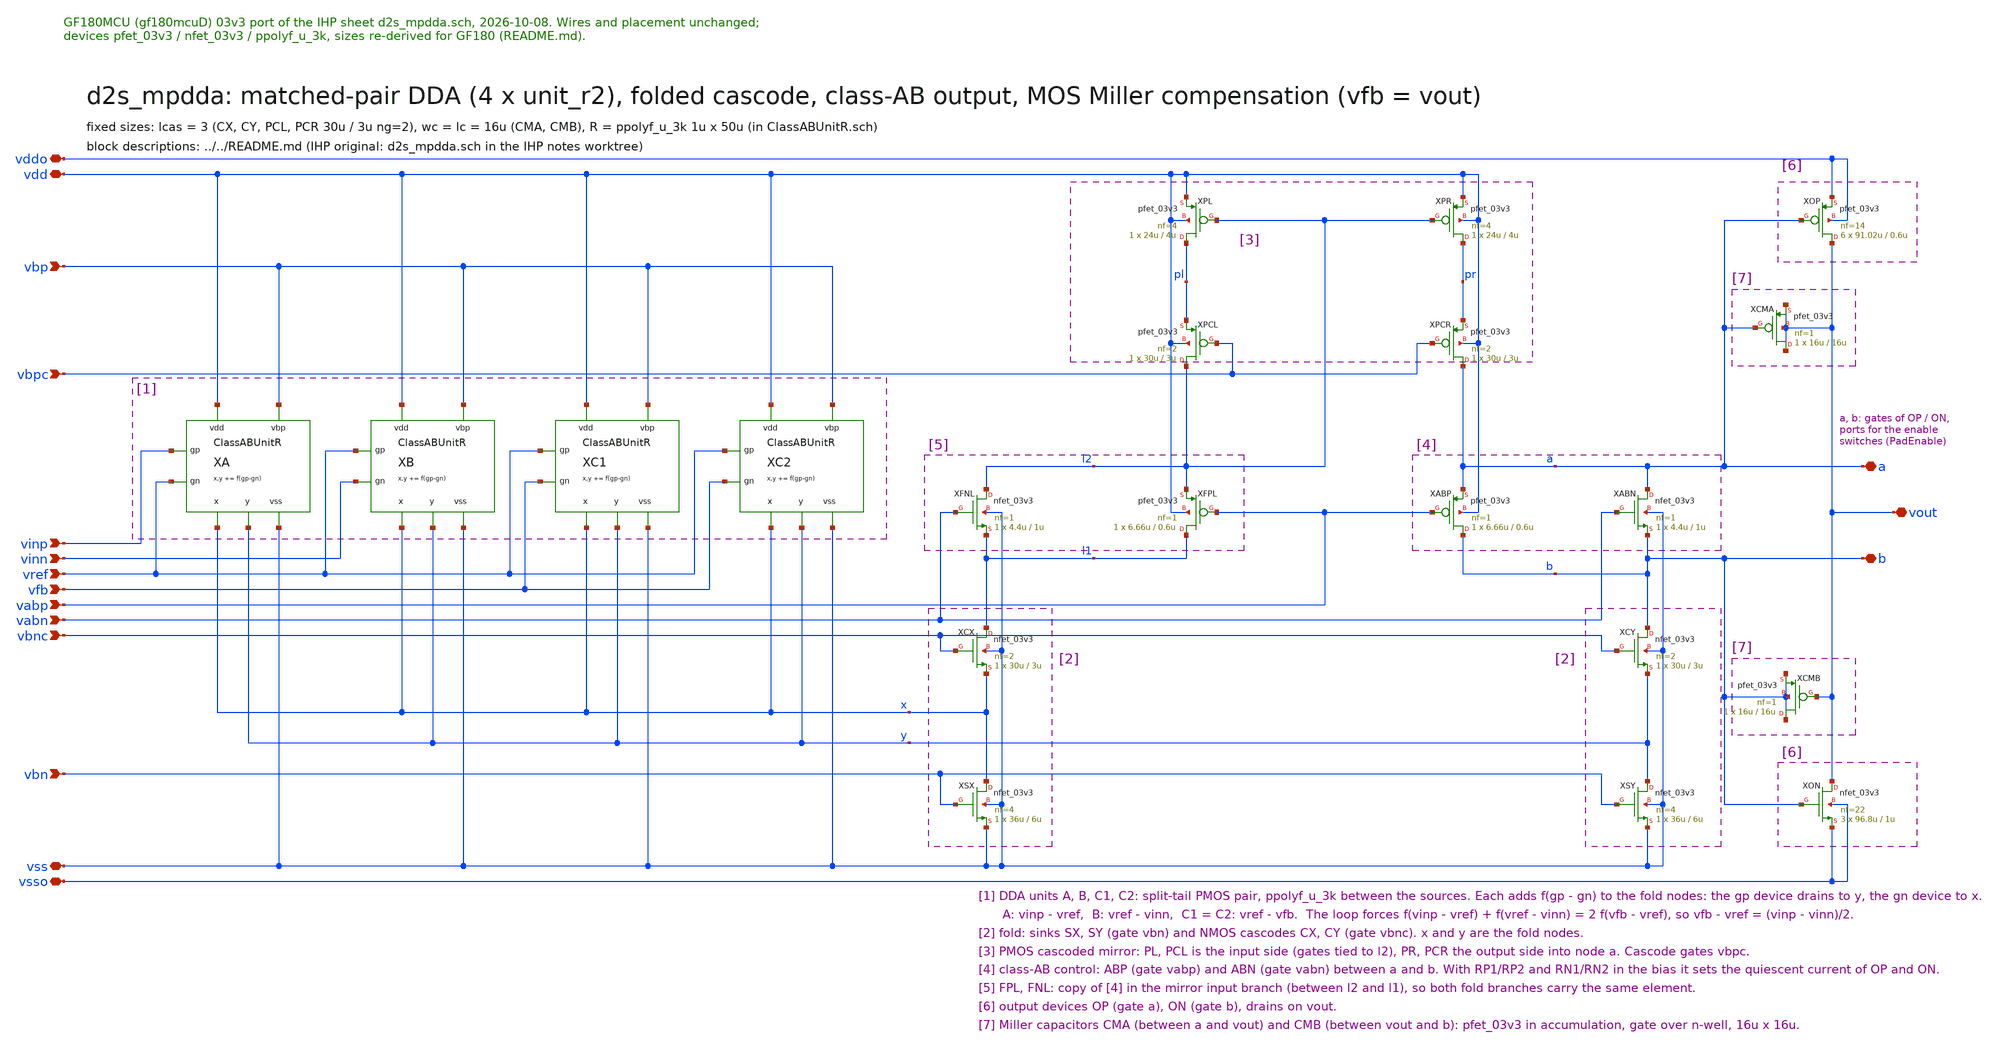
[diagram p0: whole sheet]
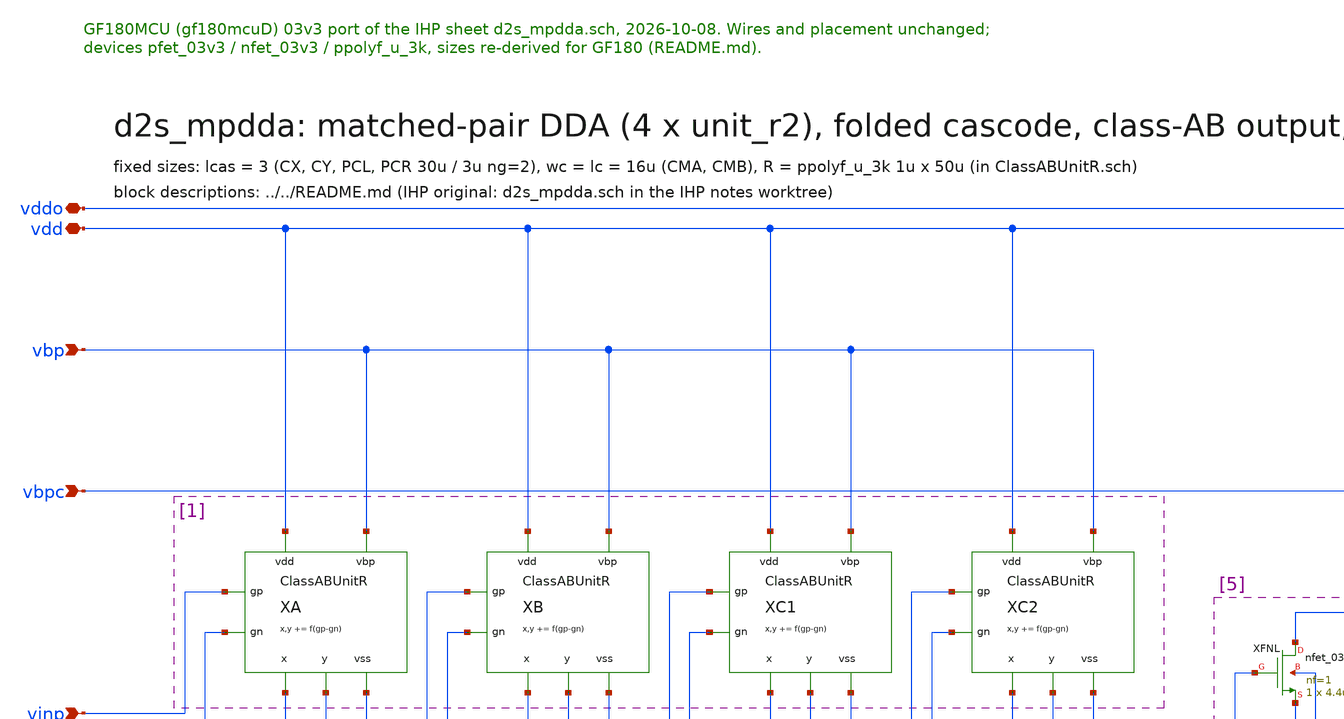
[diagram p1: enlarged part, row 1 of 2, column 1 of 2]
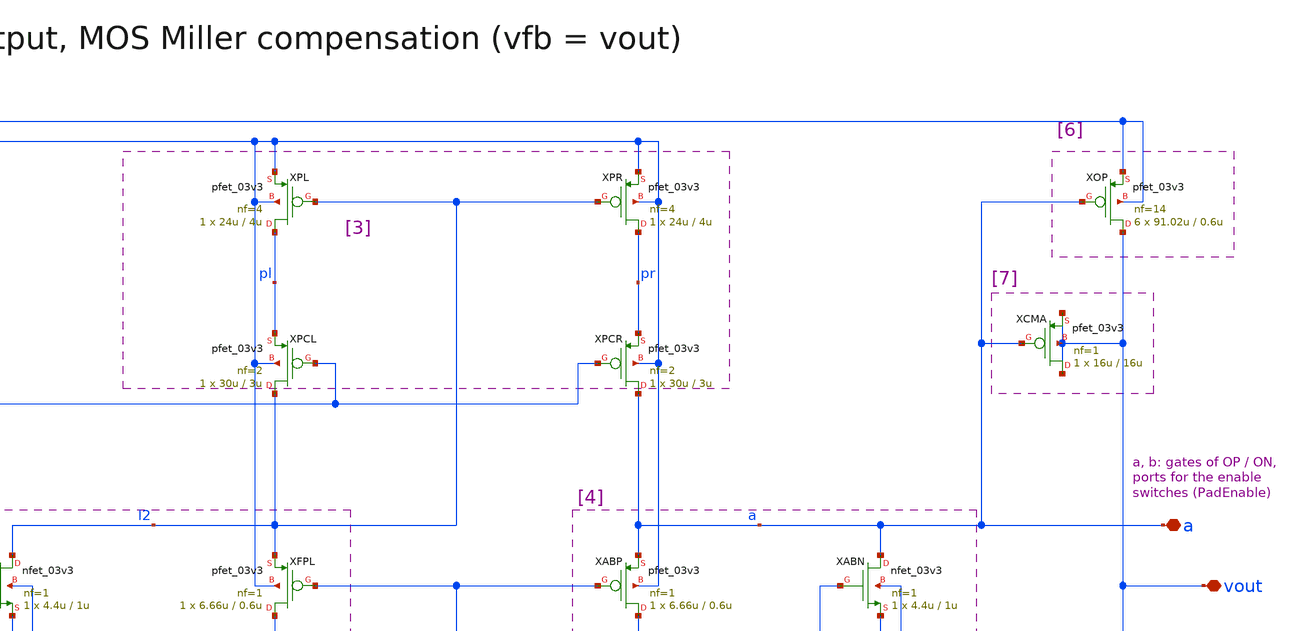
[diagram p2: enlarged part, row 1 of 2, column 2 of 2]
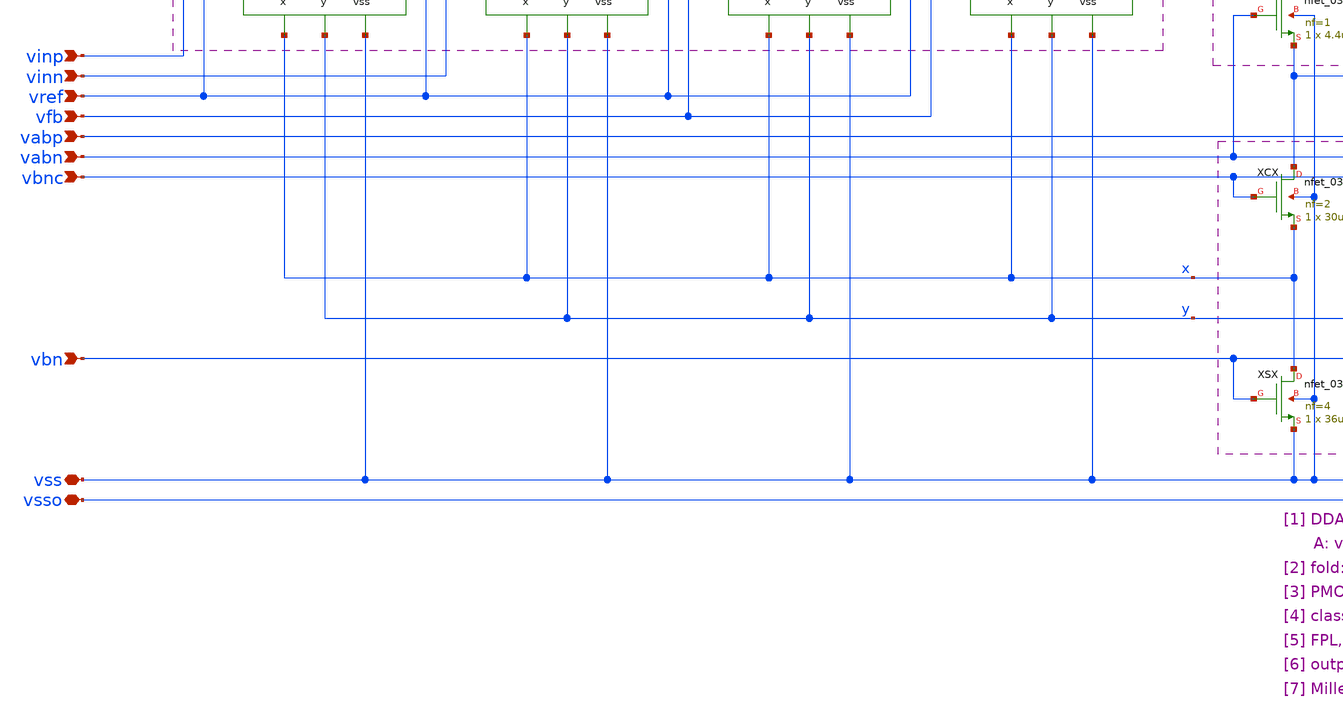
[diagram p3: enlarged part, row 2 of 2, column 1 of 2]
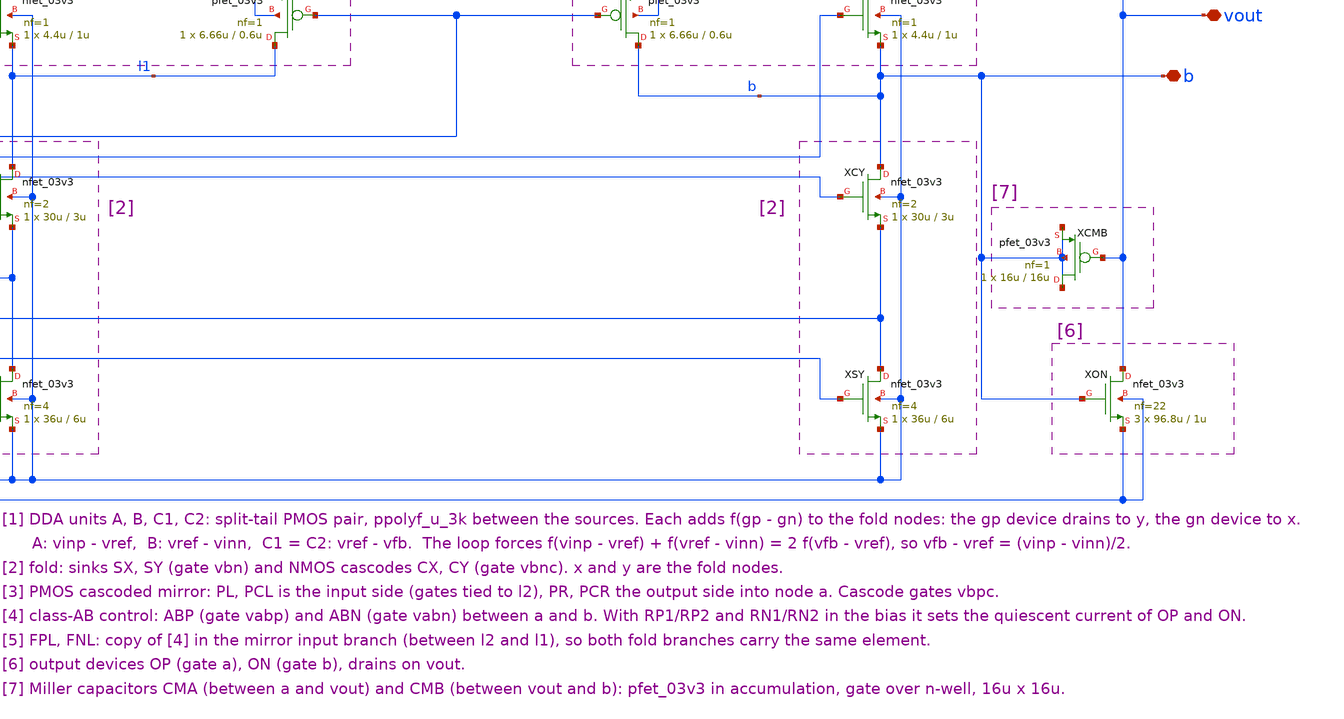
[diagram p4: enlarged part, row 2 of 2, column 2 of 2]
** sch_path: macros/ClassABDriver/schematic/xschem/ClassABDriver.sch
**.subckt ClassABDriver vdd vss vddo vsso vinp vinn vref vout vfb vbp vbn vbpc vbnc vabp vabn a b
*.iopin vdd
*.iopin vss
*.iopin vddo
*.iopin vsso
*.ipin vinp
*.ipin vinn
*.ipin vref
*.iopin vout
*.ipin vfb
*.ipin vbp
*.ipin vbn
*.ipin vbpc
*.ipin vbnc
*.ipin vabp
*.ipin vabn
*.iopin a
*.iopin b
XA x y vinp vref vdd vss vbp ClassABUnitR
XB x y vref vinn vdd vss vbp ClassABUnitR
XC1 x y vref vfb vdd vss vbp ClassABUnitR
XC2 x y vref vfb vdd vss vbp ClassABUnitR
XFNL l2 vabn l1 vss nfet_03v3 L=1u W=4.4u nf=1 ad='int((nf+1)/2) * W/nf * 0.18u' as='int((nf+2)/2) * W/nf * 0.18u'
+ pd='2*int((nf+1)/2) * (W/nf + 0.18u)' ps='2*int((nf+2)/2) * (W/nf + 0.18u)' nrd='0.18u / W' nrs='0.18u / W'
+ sa=0 sb=0 sd=0 m=1
XCX l1 vbnc x vss nfet_03v3 L=3u W=30u nf=2 ad='int((nf+1)/2) * W/nf * 0.18u' as='int((nf+2)/2) * W/nf * 0.18u'
+ pd='2*int((nf+1)/2) * (W/nf + 0.18u)' ps='2*int((nf+2)/2) * (W/nf + 0.18u)' nrd='0.18u / W' nrs='0.18u / W'
+ sa=0 sb=0 sd=0 m=1
XSX x vbn vss vss nfet_03v3 L=6u W=36u nf=4 ad='int((nf+1)/2) * W/nf * 0.18u' as='int((nf+2)/2) * W/nf * 0.18u'
+ pd='2*int((nf+1)/2) * (W/nf + 0.18u)' ps='2*int((nf+2)/2) * (W/nf + 0.18u)' nrd='0.18u / W' nrs='0.18u / W'
+ sa=0 sb=0 sd=0 m=1
XPL pl l2 vdd vdd pfet_03v3 L=4u W=24u nf=4 ad='int((nf+1)/2) * W/nf * 0.18u' as='int((nf+2)/2) * W/nf * 0.18u'
+ pd='2*int((nf+1)/2) * (W/nf + 0.18u)' ps='2*int((nf+2)/2) * (W/nf + 0.18u)' nrd='0.18u / W' nrs='0.18u / W'
+ sa=0 sb=0 sd=0 m=1
XPCL l2 vbpc pl vdd pfet_03v3 L=3u W=30u nf=2 ad='int((nf+1)/2) * W/nf * 0.18u' as='int((nf+2)/2) * W/nf * 0.18u'
+ pd='2*int((nf+1)/2) * (W/nf + 0.18u)' ps='2*int((nf+2)/2) * (W/nf + 0.18u)' nrd='0.18u / W' nrs='0.18u / W'
+ sa=0 sb=0 sd=0 m=1
XFPL l1 vabp l2 vdd pfet_03v3 L=0.6u W=6.66u nf=1 ad='int((nf+1)/2) * W/nf * 0.18u' as='int((nf+2)/2) * W/nf * 0.18u'
+ pd='2*int((nf+1)/2) * (W/nf + 0.18u)' ps='2*int((nf+2)/2) * (W/nf + 0.18u)' nrd='0.18u / W' nrs='0.18u / W'
+ sa=0 sb=0 sd=0 m=1
XPR pr l2 vdd vdd pfet_03v3 L=4u W=24u nf=4 ad='int((nf+1)/2) * W/nf * 0.18u' as='int((nf+2)/2) * W/nf * 0.18u'
+ pd='2*int((nf+1)/2) * (W/nf + 0.18u)' ps='2*int((nf+2)/2) * (W/nf + 0.18u)' nrd='0.18u / W' nrs='0.18u / W'
+ sa=0 sb=0 sd=0 m=1
XPCR a vbpc pr vdd pfet_03v3 L=3u W=30u nf=2 ad='int((nf+1)/2) * W/nf * 0.18u' as='int((nf+2)/2) * W/nf * 0.18u'
+ pd='2*int((nf+1)/2) * (W/nf + 0.18u)' ps='2*int((nf+2)/2) * (W/nf + 0.18u)' nrd='0.18u / W' nrs='0.18u / W'
+ sa=0 sb=0 sd=0 m=1
XABP b vabp a vdd pfet_03v3 L=0.6u W=6.66u nf=1 ad='int((nf+1)/2) * W/nf * 0.18u' as='int((nf+2)/2) * W/nf * 0.18u'
+ pd='2*int((nf+1)/2) * (W/nf + 0.18u)' ps='2*int((nf+2)/2) * (W/nf + 0.18u)' nrd='0.18u / W' nrs='0.18u / W'
+ sa=0 sb=0 sd=0 m=1
XABN a vabn b vss nfet_03v3 L=1u W=4.4u nf=1 ad='int((nf+1)/2) * W/nf * 0.18u' as='int((nf+2)/2) * W/nf * 0.18u'
+ pd='2*int((nf+1)/2) * (W/nf + 0.18u)' ps='2*int((nf+2)/2) * (W/nf + 0.18u)' nrd='0.18u / W' nrs='0.18u / W'
+ sa=0 sb=0 sd=0 m=1
XCY b vbnc y vss nfet_03v3 L=3u W=30u nf=2 ad='int((nf+1)/2) * W/nf * 0.18u' as='int((nf+2)/2) * W/nf * 0.18u'
+ pd='2*int((nf+1)/2) * (W/nf + 0.18u)' ps='2*int((nf+2)/2) * (W/nf + 0.18u)' nrd='0.18u / W' nrs='0.18u / W'
+ sa=0 sb=0 sd=0 m=1
XSY y vbn vss vss nfet_03v3 L=6u W=36u nf=4 ad='int((nf+1)/2) * W/nf * 0.18u' as='int((nf+2)/2) * W/nf * 0.18u'
+ pd='2*int((nf+1)/2) * (W/nf + 0.18u)' ps='2*int((nf+2)/2) * (W/nf + 0.18u)' nrd='0.18u / W' nrs='0.18u / W'
+ sa=0 sb=0 sd=0 m=1
XOP vout a vddo vddo pfet_03v3 L=0.6u W=91.02u nf=14 ad='int((nf+1)/2) * W/nf * 0.18u' as='int((nf+2)/2) * W/nf * 0.18u'
+ pd='2*int((nf+1)/2) * (W/nf + 0.18u)' ps='2*int((nf+2)/2) * (W/nf + 0.18u)' nrd='0.18u / W' nrs='0.18u / W'
+ sa=0 sb=0 sd=0 m=6
XON vout b vsso vsso nfet_03v3 L=1u W=96.8u nf=22 ad='int((nf+1)/2) * W/nf * 0.18u' as='int((nf+2)/2) * W/nf * 0.18u'
+ pd='2*int((nf+1)/2) * (W/nf + 0.18u)' ps='2*int((nf+2)/2) * (W/nf + 0.18u)' nrd='0.18u / W' nrs='0.18u / W'
+ sa=0 sb=0 sd=0 m=3
XCMA vout a vout vout pfet_03v3 L=16u W=16u nf=1 ad='int((nf+1)/2) * W/nf * 0.18u' as='int((nf+2)/2) * W/nf * 0.18u'
+ pd='2*int((nf+1)/2) * (W/nf + 0.18u)' ps='2*int((nf+2)/2) * (W/nf + 0.18u)' nrd='0.18u / W' nrs='0.18u / W'
+ sa=0 sb=0 sd=0 m=1
XCMB b vout b b pfet_03v3 L=16u W=16u nf=1 ad='int((nf+1)/2) * W/nf * 0.18u' as='int((nf+2)/2) * W/nf * 0.18u'
+ pd='2*int((nf+1)/2) * (W/nf + 0.18u)' ps='2*int((nf+2)/2) * (W/nf + 0.18u)' nrd='0.18u / W' nrs='0.18u / W'
+ sa=0 sb=0 sd=0 m=1
**.ends

* expanding   symbol:  ClassABUnitR.sym # of pins=7
** sym_path: macros/ClassABDriver/schematic/xschem/ClassABUnitR.sym
** sch_path: macros/ClassABDriver/schematic/xschem/ClassABUnitR.sch
.subckt ClassABUnitR x y gp gn vdd vss vbp
*.opin x
*.opin y
*.ipin gp
*.ipin gn
*.iopin vdd
*.iopin vss
*.ipin vbp
XTa sa vbp vdd vdd pfet_03v3 L=6u W=20u nf=2 ad='int((nf+1)/2) * W/nf * 0.18u' as='int((nf+2)/2) * W/nf * 0.18u'
+ pd='2*int((nf+1)/2) * (W/nf + 0.18u)' ps='2*int((nf+2)/2) * (W/nf + 0.18u)' nrd='0.18u / W' nrs='0.18u / W'
+ sa=0 sb=0 sd=0 m=1
XTb sb vbp vdd vdd pfet_03v3 L=6u W=20u nf=2 ad='int((nf+1)/2) * W/nf * 0.18u' as='int((nf+2)/2) * W/nf * 0.18u'
+ pd='2*int((nf+1)/2) * (W/nf + 0.18u)' ps='2*int((nf+2)/2) * (W/nf + 0.18u)' nrd='0.18u / W' nrs='0.18u / W'
+ sa=0 sb=0 sd=0 m=1
XMa y gp sa sa pfet_03v3 L=1u W=20u nf=2 ad='int((nf+1)/2) * W/nf * 0.18u' as='int((nf+2)/2) * W/nf * 0.18u'
+ pd='2*int((nf+1)/2) * (W/nf + 0.18u)' ps='2*int((nf+2)/2) * (W/nf + 0.18u)' nrd='0.18u / W' nrs='0.18u / W'
+ sa=0 sb=0 sd=0 m=1
XMb x gn sb sb pfet_03v3 L=1u W=20u nf=2 ad='int((nf+1)/2) * W/nf * 0.18u' as='int((nf+2)/2) * W/nf * 0.18u'
+ pd='2*int((nf+1)/2) * (W/nf + 0.18u)' ps='2*int((nf+2)/2) * (W/nf + 0.18u)' nrd='0.18u / W' nrs='0.18u / W'
+ sa=0 sb=0 sd=0 m=1
XR sb sa vss ppolyf_u_3k r_width=1u r_length=50u m=1
.ends

.end
